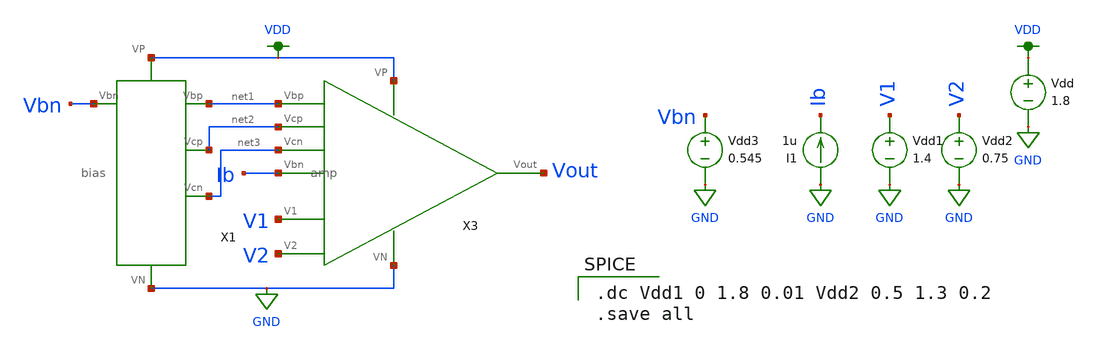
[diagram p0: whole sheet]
** sch_path: mp3/schematic/lds/amp_tran_lds.sch
**.subckt amp_tran_lds
Vdd1 V1 GND 1.4
Vdd2 V2 GND 0.75
I1 GND Ib 1u
Vdd VDD GND 1.8
Vdd3 Vbn GND 0.545
X3 VDD GND Ib net3 net2 net1 V1 V2 Vout amp
X1 VDD GND Vbn net1 net2 net3 bias
**** begin user architecture code

.option wnflag=1
.lib ~/skywater/skywater-pdk/libraries/sky130_fd_pr_ngspice/latest/models/sky130.lib.spice tt


.dc Vdd1 0 1.8 0.01 Vdd2 0.5 1.3 0.2
.save all

**** end user architecture code
**.ends

* expanding   symbol:  /home/madvlsi/madvlsi/mp3/schematic/lds/amp.sym # of pins=9
** sym_path: mp3/schematic/lds/amp.sym
** sch_path: mp3/schematic/lds/amp.sch
.subckt amp VP VN Vbn Vcn Vcp Vbp V1 V2 Vout
*.iopin VP
*.iopin VN
*.opin Vout
*.ipin V1
*.ipin V2
*.ipin Vbp
*.ipin Vcp
*.iopin Vbn
*.ipin Vcn
XM95 net2 Vcp net1 VDD sky130_fd_pr__pfet_01v8 L=0.5 W=6 nf=1 ad='int((nf+1)/2) * W/nf * 0.29' as='int((nf+2)/2) * W/nf * 0.29'
+ pd='2*int((nf+1)/2) * (W/nf + 0.29)' ps='2*int((nf+2)/2) * (W/nf + 0.29)' nrd='0.29 / W' nrs='0.29 / W'
+ sa=0 sb=0 sd=0 mult=1 m=1
XM96 net1 Vcp net2 VDD sky130_fd_pr__pfet_01v8 L=0.5 W=6 nf=1 ad='int((nf+1)/2) * W/nf * 0.29' as='int((nf+2)/2) * W/nf * 0.29'
+ pd='2*int((nf+1)/2) * (W/nf + 0.29)' ps='2*int((nf+2)/2) * (W/nf + 0.29)' nrd='0.29 / W' nrs='0.29 / W'
+ sa=0 sb=0 sd=0 mult=1 m=1
XM911 VP Vbp net2 VDD sky130_fd_pr__pfet_01v8 L=0.5 W=6 nf=1 ad='int((nf+1)/2) * W/nf * 0.29' as='int((nf+2)/2) * W/nf * 0.29'
+ pd='2*int((nf+1)/2) * (W/nf + 0.29)' ps='2*int((nf+2)/2) * (W/nf + 0.29)' nrd='0.29 / W' nrs='0.29 / W'
+ sa=0 sb=0 sd=0 mult=1 m=1
XM912 net2 Vbp VP VDD sky130_fd_pr__pfet_01v8 L=0.5 W=6 nf=1 ad='int((nf+1)/2) * W/nf * 0.29' as='int((nf+2)/2) * W/nf * 0.29'
+ pd='2*int((nf+1)/2) * (W/nf + 0.29)' ps='2*int((nf+2)/2) * (W/nf + 0.29)' nrd='0.29 / W' nrs='0.29 / W'
+ sa=0 sb=0 sd=0 mult=1 m=1
XM913 VP Vbp net3 VDD sky130_fd_pr__pfet_01v8 L=0.5 W=6 nf=1 ad='int((nf+1)/2) * W/nf * 0.29' as='int((nf+2)/2) * W/nf * 0.29'
+ pd='2*int((nf+1)/2) * (W/nf + 0.29)' ps='2*int((nf+2)/2) * (W/nf + 0.29)' nrd='0.29 / W' nrs='0.29 / W'
+ sa=0 sb=0 sd=0 mult=1 m=1
XM914 net3 Vbp VP VDD sky130_fd_pr__pfet_01v8 L=0.5 W=6 nf=1 ad='int((nf+1)/2) * W/nf * 0.29' as='int((nf+2)/2) * W/nf * 0.29'
+ pd='2*int((nf+1)/2) * (W/nf + 0.29)' ps='2*int((nf+2)/2) * (W/nf + 0.29)' nrd='0.29 / W' nrs='0.29 / W'
+ sa=0 sb=0 sd=0 mult=1 m=1
XM915 net3 Vcp Vout VDD sky130_fd_pr__pfet_01v8 L=0.5 W=6 nf=1 ad='int((nf+1)/2) * W/nf * 0.29' as='int((nf+2)/2) * W/nf * 0.29'
+ pd='2*int((nf+1)/2) * (W/nf + 0.29)' ps='2*int((nf+2)/2) * (W/nf + 0.29)' nrd='0.29 / W' nrs='0.29 / W'
+ sa=0 sb=0 sd=0 mult=1 m=1
XM916 Vout Vcp net3 VDD sky130_fd_pr__pfet_01v8 L=0.5 W=6 nf=1 ad='int((nf+1)/2) * W/nf * 0.29' as='int((nf+2)/2) * W/nf * 0.29'
+ pd='2*int((nf+1)/2) * (W/nf + 0.29)' ps='2*int((nf+2)/2) * (W/nf + 0.29)' nrd='0.29 / W' nrs='0.29 / W'
+ sa=0 sb=0 sd=0 mult=1 m=1
XM917 net2 V1 net4 GND sky130_fd_pr__nfet_01v8 L=0.5 W=3 nf=1 ad='int((nf+1)/2) * W/nf * 0.29' as='int((nf+2)/2) * W/nf * 0.29'
+ pd='2*int((nf+1)/2) * (W/nf + 0.29)' ps='2*int((nf+2)/2) * (W/nf + 0.29)' nrd='0.29 / W' nrs='0.29 / W'
+ sa=0 sb=0 sd=0 mult=1 m=1
XM918 net4 V1 net2 GND sky130_fd_pr__nfet_01v8 L=0.5 W=3 nf=1 ad='int((nf+1)/2) * W/nf * 0.29' as='int((nf+2)/2) * W/nf * 0.29'
+ pd='2*int((nf+1)/2) * (W/nf + 0.29)' ps='2*int((nf+2)/2) * (W/nf + 0.29)' nrd='0.29 / W' nrs='0.29 / W'
+ sa=0 sb=0 sd=0 mult=1 m=1
XM919 net2 V1 net4 GND sky130_fd_pr__nfet_01v8 L=0.5 W=3 nf=1 ad='int((nf+1)/2) * W/nf * 0.29' as='int((nf+2)/2) * W/nf * 0.29'
+ pd='2*int((nf+1)/2) * (W/nf + 0.29)' ps='2*int((nf+2)/2) * (W/nf + 0.29)' nrd='0.29 / W' nrs='0.29 / W'
+ sa=0 sb=0 sd=0 mult=1 m=1
XM920 net4 V1 net2 GND sky130_fd_pr__nfet_01v8 L=0.5 W=3 nf=1 ad='int((nf+1)/2) * W/nf * 0.29' as='int((nf+2)/2) * W/nf * 0.29'
+ pd='2*int((nf+1)/2) * (W/nf + 0.29)' ps='2*int((nf+2)/2) * (W/nf + 0.29)' nrd='0.29 / W' nrs='0.29 / W'
+ sa=0 sb=0 sd=0 mult=1 m=1
XM921 net3 V2 net4 GND sky130_fd_pr__nfet_01v8 L=0.5 W=3 nf=1 ad='int((nf+1)/2) * W/nf * 0.29' as='int((nf+2)/2) * W/nf * 0.29'
+ pd='2*int((nf+1)/2) * (W/nf + 0.29)' ps='2*int((nf+2)/2) * (W/nf + 0.29)' nrd='0.29 / W' nrs='0.29 / W'
+ sa=0 sb=0 sd=0 mult=1 m=1
XM922 net4 V2 net3 GND sky130_fd_pr__nfet_01v8 L=0.5 W=3 nf=1 ad='int((nf+1)/2) * W/nf * 0.29' as='int((nf+2)/2) * W/nf * 0.29'
+ pd='2*int((nf+1)/2) * (W/nf + 0.29)' ps='2*int((nf+2)/2) * (W/nf + 0.29)' nrd='0.29 / W' nrs='0.29 / W'
+ sa=0 sb=0 sd=0 mult=1 m=1
XM923 net3 V2 net4 GND sky130_fd_pr__nfet_01v8 L=0.5 W=3 nf=1 ad='int((nf+1)/2) * W/nf * 0.29' as='int((nf+2)/2) * W/nf * 0.29'
+ pd='2*int((nf+1)/2) * (W/nf + 0.29)' ps='2*int((nf+2)/2) * (W/nf + 0.29)' nrd='0.29 / W' nrs='0.29 / W'
+ sa=0 sb=0 sd=0 mult=1 m=1
XM94 net4 V2 net3 GND sky130_fd_pr__nfet_01v8 L=0.5 W=3 nf=1 ad='int((nf+1)/2) * W/nf * 0.29' as='int((nf+2)/2) * W/nf * 0.29'
+ pd='2*int((nf+1)/2) * (W/nf + 0.29)' ps='2*int((nf+2)/2) * (W/nf + 0.29)' nrd='0.29 / W' nrs='0.29 / W'
+ sa=0 sb=0 sd=0 mult=1 m=1
XM925 VN Vbn Vbn GND sky130_fd_pr__nfet_01v8 L=0.5 W=6 nf=1 ad='int((nf+1)/2) * W/nf * 0.29' as='int((nf+2)/2) * W/nf * 0.29'
+ pd='2*int((nf+1)/2) * (W/nf + 0.29)' ps='2*int((nf+2)/2) * (W/nf + 0.29)' nrd='0.29 / W' nrs='0.29 / W'
+ sa=0 sb=0 sd=0 mult=1 m=1
XM926 Vbn Vbn VN GND sky130_fd_pr__nfet_01v8 L=0.5 W=6 nf=1 ad='int((nf+1)/2) * W/nf * 0.29' as='int((nf+2)/2) * W/nf * 0.29'
+ pd='2*int((nf+1)/2) * (W/nf + 0.29)' ps='2*int((nf+2)/2) * (W/nf + 0.29)' nrd='0.29 / W' nrs='0.29 / W'
+ sa=0 sb=0 sd=0 mult=1 m=1
XM927 VN Vbn net4 GND sky130_fd_pr__nfet_01v8 L=0.5 W=6 nf=1 ad='int((nf+1)/2) * W/nf * 0.29' as='int((nf+2)/2) * W/nf * 0.29'
+ pd='2*int((nf+1)/2) * (W/nf + 0.29)' ps='2*int((nf+2)/2) * (W/nf + 0.29)' nrd='0.29 / W' nrs='0.29 / W'
+ sa=0 sb=0 sd=0 mult=1 m=1
XM928 net4 Vbn VN GND sky130_fd_pr__nfet_01v8 L=0.5 W=6 nf=1 ad='int((nf+1)/2) * W/nf * 0.29' as='int((nf+2)/2) * W/nf * 0.29'
+ pd='2*int((nf+1)/2) * (W/nf + 0.29)' ps='2*int((nf+2)/2) * (W/nf + 0.29)' nrd='0.29 / W' nrs='0.29 / W'
+ sa=0 sb=0 sd=0 mult=1 m=1
XM929 VN Vbn Vbn GND sky130_fd_pr__nfet_01v8 L=0.5 W=6 nf=1 ad='int((nf+1)/2) * W/nf * 0.29' as='int((nf+2)/2) * W/nf * 0.29'
+ pd='2*int((nf+1)/2) * (W/nf + 0.29)' ps='2*int((nf+2)/2) * (W/nf + 0.29)' nrd='0.29 / W' nrs='0.29 / W'
+ sa=0 sb=0 sd=0 mult=1 m=1
XM930 Vbn Vbn VN GND sky130_fd_pr__nfet_01v8 L=0.5 W=6 nf=1 ad='int((nf+1)/2) * W/nf * 0.29' as='int((nf+2)/2) * W/nf * 0.29'
+ pd='2*int((nf+1)/2) * (W/nf + 0.29)' ps='2*int((nf+2)/2) * (W/nf + 0.29)' nrd='0.29 / W' nrs='0.29 / W'
+ sa=0 sb=0 sd=0 mult=1 m=1
XM931 VN Vbn net4 GND sky130_fd_pr__nfet_01v8 L=0.5 W=6 nf=1 ad='int((nf+1)/2) * W/nf * 0.29' as='int((nf+2)/2) * W/nf * 0.29'
+ pd='2*int((nf+1)/2) * (W/nf + 0.29)' ps='2*int((nf+2)/2) * (W/nf + 0.29)' nrd='0.29 / W' nrs='0.29 / W'
+ sa=0 sb=0 sd=0 mult=1 m=1
XM932 net4 Vbn VN GND sky130_fd_pr__nfet_01v8 L=0.5 W=6 nf=1 ad='int((nf+1)/2) * W/nf * 0.29' as='int((nf+2)/2) * W/nf * 0.29'
+ pd='2*int((nf+1)/2) * (W/nf + 0.29)' ps='2*int((nf+2)/2) * (W/nf + 0.29)' nrd='0.29 / W' nrs='0.29 / W'
+ sa=0 sb=0 sd=0 mult=1 m=1
XM933 net5 Vcn net1 GND sky130_fd_pr__nfet_01v8 L=0.5 W=6 nf=1 ad='int((nf+1)/2) * W/nf * 0.29' as='int((nf+2)/2) * W/nf * 0.29'
+ pd='2*int((nf+1)/2) * (W/nf + 0.29)' ps='2*int((nf+2)/2) * (W/nf + 0.29)' nrd='0.29 / W' nrs='0.29 / W'
+ sa=0 sb=0 sd=0 mult=1 m=1
XM934 net1 Vcn net5 GND sky130_fd_pr__nfet_01v8 L=0.5 W=6 nf=1 ad='int((nf+1)/2) * W/nf * 0.29' as='int((nf+2)/2) * W/nf * 0.29'
+ pd='2*int((nf+1)/2) * (W/nf + 0.29)' ps='2*int((nf+2)/2) * (W/nf + 0.29)' nrd='0.29 / W' nrs='0.29 / W'
+ sa=0 sb=0 sd=0 mult=1 m=1
XM935 net5 net1 VN GND sky130_fd_pr__nfet_01v8 L=0.5 W=6 nf=1 ad='int((nf+1)/2) * W/nf * 0.29' as='int((nf+2)/2) * W/nf * 0.29'
+ pd='2*int((nf+1)/2) * (W/nf + 0.29)' ps='2*int((nf+2)/2) * (W/nf + 0.29)' nrd='0.29 / W' nrs='0.29 / W'
+ sa=0 sb=0 sd=0 mult=1 m=1
XM936 VN net1 net5 GND sky130_fd_pr__nfet_01v8 L=0.5 W=6 nf=1 ad='int((nf+1)/2) * W/nf * 0.29' as='int((nf+2)/2) * W/nf * 0.29'
+ pd='2*int((nf+1)/2) * (W/nf + 0.29)' ps='2*int((nf+2)/2) * (W/nf + 0.29)' nrd='0.29 / W' nrs='0.29 / W'
+ sa=0 sb=0 sd=0 mult=1 m=1
XM937 net6 Vcn Vout GND sky130_fd_pr__nfet_01v8 L=0.5 W=6 nf=1 ad='int((nf+1)/2) * W/nf * 0.29' as='int((nf+2)/2) * W/nf * 0.29'
+ pd='2*int((nf+1)/2) * (W/nf + 0.29)' ps='2*int((nf+2)/2) * (W/nf + 0.29)' nrd='0.29 / W' nrs='0.29 / W'
+ sa=0 sb=0 sd=0 mult=1 m=1
XM938 Vout Vcn net6 GND sky130_fd_pr__nfet_01v8 L=0.5 W=6 nf=1 ad='int((nf+1)/2) * W/nf * 0.29' as='int((nf+2)/2) * W/nf * 0.29'
+ pd='2*int((nf+1)/2) * (W/nf + 0.29)' ps='2*int((nf+2)/2) * (W/nf + 0.29)' nrd='0.29 / W' nrs='0.29 / W'
+ sa=0 sb=0 sd=0 mult=1 m=1
XM939 net6 net1 VN GND sky130_fd_pr__nfet_01v8 L=0.5 W=6 nf=1 ad='int((nf+1)/2) * W/nf * 0.29' as='int((nf+2)/2) * W/nf * 0.29'
+ pd='2*int((nf+1)/2) * (W/nf + 0.29)' ps='2*int((nf+2)/2) * (W/nf + 0.29)' nrd='0.29 / W' nrs='0.29 / W'
+ sa=0 sb=0 sd=0 mult=1 m=1
XM940 VN net1 net6 GND sky130_fd_pr__nfet_01v8 L=0.5 W=6 nf=1 ad='int((nf+1)/2) * W/nf * 0.29' as='int((nf+2)/2) * W/nf * 0.29'
+ pd='2*int((nf+1)/2) * (W/nf + 0.29)' ps='2*int((nf+2)/2) * (W/nf + 0.29)' nrd='0.29 / W' nrs='0.29 / W'
+ sa=0 sb=0 sd=0 mult=1 m=1
XM1 VN VN Vbn GND sky130_fd_pr__nfet_01v8 L=0.5 W=6 nf=1 ad='int((nf+1)/2) * W/nf * 0.29' as='int((nf+2)/2) * W/nf * 0.29'
+ pd='2*int((nf+1)/2) * (W/nf + 0.29)' ps='2*int((nf+2)/2) * (W/nf + 0.29)' nrd='0.29 / W' nrs='0.29 / W'
+ sa=0 sb=0 sd=0 mult=1 m=1
XM2 net1 VN VN GND sky130_fd_pr__nfet_01v8 L=0.5 W=6 nf=1 ad='int((nf+1)/2) * W/nf * 0.29' as='int((nf+2)/2) * W/nf * 0.29'
+ pd='2*int((nf+1)/2) * (W/nf + 0.29)' ps='2*int((nf+2)/2) * (W/nf + 0.29)' nrd='0.29 / W' nrs='0.29 / W'
+ sa=0 sb=0 sd=0 mult=1 m=1
XM3 VN VN net4 GND sky130_fd_pr__nfet_01v8 L=0.5 W=3 nf=1 ad='int((nf+1)/2) * W/nf * 0.29' as='int((nf+2)/2) * W/nf * 0.29'
+ pd='2*int((nf+1)/2) * (W/nf + 0.29)' ps='2*int((nf+2)/2) * (W/nf + 0.29)' nrd='0.29 / W' nrs='0.29 / W'
+ sa=0 sb=0 sd=0 mult=1 m=1
XM4 VP VP net2 VDD sky130_fd_pr__pfet_01v8 L=0.5 W=6 nf=1 ad='int((nf+1)/2) * W/nf * 0.29' as='int((nf+2)/2) * W/nf * 0.29'
+ pd='2*int((nf+1)/2) * (W/nf + 0.29)' ps='2*int((nf+2)/2) * (W/nf + 0.29)' nrd='0.29 / W' nrs='0.29 / W'
+ sa=0 sb=0 sd=0 mult=1 m=1
XM5 net3 VP VP VDD sky130_fd_pr__pfet_01v8 L=0.5 W=6 nf=1 ad='int((nf+1)/2) * W/nf * 0.29' as='int((nf+2)/2) * W/nf * 0.29'
+ pd='2*int((nf+1)/2) * (W/nf + 0.29)' ps='2*int((nf+2)/2) * (W/nf + 0.29)' nrd='0.29 / W' nrs='0.29 / W'
+ sa=0 sb=0 sd=0 mult=1 m=1
XM6 net4 VN VN GND sky130_fd_pr__nfet_01v8 L=0.5 W=3 nf=1 ad='int((nf+1)/2) * W/nf * 0.29' as='int((nf+2)/2) * W/nf * 0.29'
+ pd='2*int((nf+1)/2) * (W/nf + 0.29)' ps='2*int((nf+2)/2) * (W/nf + 0.29)' nrd='0.29 / W' nrs='0.29 / W'
+ sa=0 sb=0 sd=0 mult=1 m=1
XM7 Vbn VN VN GND sky130_fd_pr__nfet_01v8 L=0.5 W=3 nf=1 ad='int((nf+1)/2) * W/nf * 0.29' as='int((nf+2)/2) * W/nf * 0.29'
+ pd='2*int((nf+1)/2) * (W/nf + 0.29)' ps='2*int((nf+2)/2) * (W/nf + 0.29)' nrd='0.29 / W' nrs='0.29 / W'
+ sa=0 sb=0 sd=0 mult=1 m=1
XM8 Vout VN VN GND sky130_fd_pr__nfet_01v8 L=0.5 W=6 nf=1 ad='int((nf+1)/2) * W/nf * 0.29' as='int((nf+2)/2) * W/nf * 0.29'
+ pd='2*int((nf+1)/2) * (W/nf + 0.29)' ps='2*int((nf+2)/2) * (W/nf + 0.29)' nrd='0.29 / W' nrs='0.29 / W'
+ sa=0 sb=0 sd=0 mult=1 m=1
.ends


* expanding   symbol:  /home/madvlsi/madvlsi/mp3/schematic/lds/bias.sym # of pins=6
** sym_path: mp3/schematic/lds/bias.sym
** sch_path: mp3/schematic/lds/bias.sch
.subckt bias VP VN Vbn Vbp Vcp Vcn
*.iopin VP
*.iopin VN
*.iopin Vbn
*.opin Vcn
*.opin Vcp
*.opin Vbp
XM1 VP Vbp net5 VDD sky130_fd_pr__pfet_01v8 L=0.5 W=6 nf=1 ad='int((nf+1)/2) * W/nf * 0.29' as='int((nf+2)/2) * W/nf * 0.29'
+ pd='2*int((nf+1)/2) * (W/nf + 0.29)' ps='2*int((nf+2)/2) * (W/nf + 0.29)' nrd='0.29 / W' nrs='0.29 / W'
+ sa=0 sb=0 sd=0 mult=1 m=1
XM2 net5 Vbp net4 VDD sky130_fd_pr__pfet_01v8 L=0.5 W=6 nf=1 ad='int((nf+1)/2) * W/nf * 0.29' as='int((nf+2)/2) * W/nf * 0.29'
+ pd='2*int((nf+1)/2) * (W/nf + 0.29)' ps='2*int((nf+2)/2) * (W/nf + 0.29)' nrd='0.29 / W' nrs='0.29 / W'
+ sa=0 sb=0 sd=0 mult=1 m=1
XM3 net4 Vbp net3 VDD sky130_fd_pr__pfet_01v8 L=0.5 W=6 nf=1 ad='int((nf+1)/2) * W/nf * 0.29' as='int((nf+2)/2) * W/nf * 0.29'
+ pd='2*int((nf+1)/2) * (W/nf + 0.29)' ps='2*int((nf+2)/2) * (W/nf + 0.29)' nrd='0.29 / W' nrs='0.29 / W'
+ sa=0 sb=0 sd=0 mult=1 m=1
XM4 net3 Vbp net2 VDD sky130_fd_pr__pfet_01v8 L=0.5 W=6 nf=1 ad='int((nf+1)/2) * W/nf * 0.29' as='int((nf+2)/2) * W/nf * 0.29'
+ pd='2*int((nf+1)/2) * (W/nf + 0.29)' ps='2*int((nf+2)/2) * (W/nf + 0.29)' nrd='0.29 / W' nrs='0.29 / W'
+ sa=0 sb=0 sd=0 mult=1 m=1
XM5 net2 Vbp net1 VDD sky130_fd_pr__pfet_01v8 L=0.5 W=6 nf=1 ad='int((nf+1)/2) * W/nf * 0.29' as='int((nf+2)/2) * W/nf * 0.29'
+ pd='2*int((nf+1)/2) * (W/nf + 0.29)' ps='2*int((nf+2)/2) * (W/nf + 0.29)' nrd='0.29 / W' nrs='0.29 / W'
+ sa=0 sb=0 sd=0 mult=1 m=1
XM6 net1 Vbp net13 VDD sky130_fd_pr__pfet_01v8 L=0.5 W=6 nf=1 ad='int((nf+1)/2) * W/nf * 0.29' as='int((nf+2)/2) * W/nf * 0.29'
+ pd='2*int((nf+1)/2) * (W/nf + 0.29)' ps='2*int((nf+2)/2) * (W/nf + 0.29)' nrd='0.29 / W' nrs='0.29 / W'
+ sa=0 sb=0 sd=0 mult=1 m=1
XM7 net7 Vbn net6 GND sky130_fd_pr__nfet_01v8 L=0.5 W=6 nf=1 ad='int((nf+1)/2) * W/nf * 0.29' as='int((nf+2)/2) * W/nf * 0.29'
+ pd='2*int((nf+1)/2) * (W/nf + 0.29)' ps='2*int((nf+2)/2) * (W/nf + 0.29)' nrd='0.29 / W' nrs='0.29 / W'
+ sa=0 sb=0 sd=0 mult=1 m=1
XM8 net6 Vbn VN GND sky130_fd_pr__nfet_01v8 L=0.5 W=6 nf=1 ad='int((nf+1)/2) * W/nf * 0.29' as='int((nf+2)/2) * W/nf * 0.29'
+ pd='2*int((nf+1)/2) * (W/nf + 0.29)' ps='2*int((nf+2)/2) * (W/nf + 0.29)' nrd='0.29 / W' nrs='0.29 / W'
+ sa=0 sb=0 sd=0 mult=1 m=1
XM9 net8 Vbn net7 GND sky130_fd_pr__nfet_01v8 L=0.5 W=6 nf=1 ad='int((nf+1)/2) * W/nf * 0.29' as='int((nf+2)/2) * W/nf * 0.29'
+ pd='2*int((nf+1)/2) * (W/nf + 0.29)' ps='2*int((nf+2)/2) * (W/nf + 0.29)' nrd='0.29 / W' nrs='0.29 / W'
+ sa=0 sb=0 sd=0 mult=1 m=1
XM10 net9 Vbn net8 GND sky130_fd_pr__nfet_01v8 L=0.5 W=6 nf=1 ad='int((nf+1)/2) * W/nf * 0.29' as='int((nf+2)/2) * W/nf * 0.29'
+ pd='2*int((nf+1)/2) * (W/nf + 0.29)' ps='2*int((nf+2)/2) * (W/nf + 0.29)' nrd='0.29 / W' nrs='0.29 / W'
+ sa=0 sb=0 sd=0 mult=1 m=1
XM11 net10 Vbn net9 GND sky130_fd_pr__nfet_01v8 L=0.5 W=6 nf=1 ad='int((nf+1)/2) * W/nf * 0.29' as='int((nf+2)/2) * W/nf * 0.29'
+ pd='2*int((nf+1)/2) * (W/nf + 0.29)' ps='2*int((nf+2)/2) * (W/nf + 0.29)' nrd='0.29 / W' nrs='0.29 / W'
+ sa=0 sb=0 sd=0 mult=1 m=1
XM12 net11 Vbn net10 GND sky130_fd_pr__nfet_01v8 L=0.5 W=6 nf=1 ad='int((nf+1)/2) * W/nf * 0.29' as='int((nf+2)/2) * W/nf * 0.29'
+ pd='2*int((nf+1)/2) * (W/nf + 0.29)' ps='2*int((nf+2)/2) * (W/nf + 0.29)' nrd='0.29 / W' nrs='0.29 / W'
+ sa=0 sb=0 sd=0 mult=1 m=1
XM13 net11 net11 net12 VDD sky130_fd_pr__pfet_01v8 L=0.5 W=6 nf=1 ad='int((nf+1)/2) * W/nf * 0.29' as='int((nf+2)/2) * W/nf * 0.29'
+ pd='2*int((nf+1)/2) * (W/nf + 0.29)' ps='2*int((nf+2)/2) * (W/nf + 0.29)' nrd='0.29 / W' nrs='0.29 / W'
+ sa=0 sb=0 sd=0 mult=1 m=1
XM14 net12 net11 net11 VDD sky130_fd_pr__pfet_01v8 L=0.5 W=6 nf=1 ad='int((nf+1)/2) * W/nf * 0.29' as='int((nf+2)/2) * W/nf * 0.29'
+ pd='2*int((nf+1)/2) * (W/nf + 0.29)' ps='2*int((nf+2)/2) * (W/nf + 0.29)' nrd='0.29 / W' nrs='0.29 / W'
+ sa=0 sb=0 sd=0 mult=1 m=1
XM15 net11 net11 net12 VDD sky130_fd_pr__pfet_01v8 L=0.5 W=6 nf=1 ad='int((nf+1)/2) * W/nf * 0.29' as='int((nf+2)/2) * W/nf * 0.29'
+ pd='2*int((nf+1)/2) * (W/nf + 0.29)' ps='2*int((nf+2)/2) * (W/nf + 0.29)' nrd='0.29 / W' nrs='0.29 / W'
+ sa=0 sb=0 sd=0 mult=1 m=1
XM16 net12 net11 net11 VDD sky130_fd_pr__pfet_01v8 L=0.5 W=6 nf=1 ad='int((nf+1)/2) * W/nf * 0.29' as='int((nf+2)/2) * W/nf * 0.29'
+ pd='2*int((nf+1)/2) * (W/nf + 0.29)' ps='2*int((nf+2)/2) * (W/nf + 0.29)' nrd='0.29 / W' nrs='0.29 / W'
+ sa=0 sb=0 sd=0 mult=1 m=1
XM17 net13 net13 net14 GND sky130_fd_pr__nfet_01v8 L=0.5 W=6 nf=1 ad='int((nf+1)/2) * W/nf * 0.29' as='int((nf+2)/2) * W/nf * 0.29'
+ pd='2*int((nf+1)/2) * (W/nf + 0.29)' ps='2*int((nf+2)/2) * (W/nf + 0.29)' nrd='0.29 / W' nrs='0.29 / W'
+ sa=0 sb=0 sd=0 mult=1 m=1
XM18 net14 net13 net13 GND sky130_fd_pr__nfet_01v8 L=0.5 W=6 nf=1 ad='int((nf+1)/2) * W/nf * 0.29' as='int((nf+2)/2) * W/nf * 0.29'
+ pd='2*int((nf+1)/2) * (W/nf + 0.29)' ps='2*int((nf+2)/2) * (W/nf + 0.29)' nrd='0.29 / W' nrs='0.29 / W'
+ sa=0 sb=0 sd=0 mult=1 m=1
XM19 net13 net13 net14 GND sky130_fd_pr__nfet_01v8 L=0.5 W=6 nf=1 ad='int((nf+1)/2) * W/nf * 0.29' as='int((nf+2)/2) * W/nf * 0.29'
+ pd='2*int((nf+1)/2) * (W/nf + 0.29)' ps='2*int((nf+2)/2) * (W/nf + 0.29)' nrd='0.29 / W' nrs='0.29 / W'
+ sa=0 sb=0 sd=0 mult=1 m=1
XM20 net14 net13 net13 GND sky130_fd_pr__nfet_01v8 L=0.5 W=6 nf=1 ad='int((nf+1)/2) * W/nf * 0.29' as='int((nf+2)/2) * W/nf * 0.29'
+ pd='2*int((nf+1)/2) * (W/nf + 0.29)' ps='2*int((nf+2)/2) * (W/nf + 0.29)' nrd='0.29 / W' nrs='0.29 / W'
+ sa=0 sb=0 sd=0 mult=1 m=1
XM21 Vcn Vbp VP VDD sky130_fd_pr__pfet_01v8 L=0.5 W=6 nf=1 ad='int((nf+1)/2) * W/nf * 0.29' as='int((nf+2)/2) * W/nf * 0.29'
+ pd='2*int((nf+1)/2) * (W/nf + 0.29)' ps='2*int((nf+2)/2) * (W/nf + 0.29)' nrd='0.29 / W' nrs='0.29 / W'
+ sa=0 sb=0 sd=0 mult=1 m=1
XM22 Vcn Vcn net14 GND sky130_fd_pr__nfet_01v8 L=0.5 W=6 nf=1 ad='int((nf+1)/2) * W/nf * 0.29' as='int((nf+2)/2) * W/nf * 0.29'
+ pd='2*int((nf+1)/2) * (W/nf + 0.29)' ps='2*int((nf+2)/2) * (W/nf + 0.29)' nrd='0.29 / W' nrs='0.29 / W'
+ sa=0 sb=0 sd=0 mult=1 m=1
XM23 VN net13 net14 GND sky130_fd_pr__nfet_01v8 L=0.5 W=6 nf=1 ad='int((nf+1)/2) * W/nf * 0.29' as='int((nf+2)/2) * W/nf * 0.29'
+ pd='2*int((nf+1)/2) * (W/nf + 0.29)' ps='2*int((nf+2)/2) * (W/nf + 0.29)' nrd='0.29 / W' nrs='0.29 / W'
+ sa=0 sb=0 sd=0 mult=1 m=1
XM24 VN Vbn Vcp GND sky130_fd_pr__nfet_01v8 L=0.5 W=6 nf=1 ad='int((nf+1)/2) * W/nf * 0.29' as='int((nf+2)/2) * W/nf * 0.29'
+ pd='2*int((nf+1)/2) * (W/nf + 0.29)' ps='2*int((nf+2)/2) * (W/nf + 0.29)' nrd='0.29 / W' nrs='0.29 / W'
+ sa=0 sb=0 sd=0 mult=1 m=1
XM25 net12 Vcp Vcp VDD sky130_fd_pr__pfet_01v8 L=0.5 W=6 nf=1 ad='int((nf+1)/2) * W/nf * 0.29' as='int((nf+2)/2) * W/nf * 0.29'
+ pd='2*int((nf+1)/2) * (W/nf + 0.29)' ps='2*int((nf+2)/2) * (W/nf + 0.29)' nrd='0.29 / W' nrs='0.29 / W'
+ sa=0 sb=0 sd=0 mult=1 m=1
XM26 net12 net11 VP VDD sky130_fd_pr__pfet_01v8 L=0.5 W=6 nf=1 ad='int((nf+1)/2) * W/nf * 0.29' as='int((nf+2)/2) * W/nf * 0.29'
+ pd='2*int((nf+1)/2) * (W/nf + 0.29)' ps='2*int((nf+2)/2) * (W/nf + 0.29)' nrd='0.29 / W' nrs='0.29 / W'
+ sa=0 sb=0 sd=0 mult=1 m=1
XM27 Vbp Vbp VP VDD sky130_fd_pr__pfet_01v8 L=0.5 W=6 nf=1 ad='int((nf+1)/2) * W/nf * 0.29' as='int((nf+2)/2) * W/nf * 0.29'
+ pd='2*int((nf+1)/2) * (W/nf + 0.29)' ps='2*int((nf+2)/2) * (W/nf + 0.29)' nrd='0.29 / W' nrs='0.29 / W'
+ sa=0 sb=0 sd=0 mult=1 m=1
XM28 VN Vbn Vbp GND sky130_fd_pr__nfet_01v8 L=0.5 W=6 nf=1 ad='int((nf+1)/2) * W/nf * 0.29' as='int((nf+2)/2) * W/nf * 0.29'
+ pd='2*int((nf+1)/2) * (W/nf + 0.29)' ps='2*int((nf+2)/2) * (W/nf + 0.29)' nrd='0.29 / W' nrs='0.29 / W'
+ sa=0 sb=0 sd=0 mult=1 m=1
XM29 VP Vbp net19 VDD sky130_fd_pr__pfet_01v8 L=0.5 W=6 nf=1 ad='int((nf+1)/2) * W/nf * 0.29' as='int((nf+2)/2) * W/nf * 0.29'
+ pd='2*int((nf+1)/2) * (W/nf + 0.29)' ps='2*int((nf+2)/2) * (W/nf + 0.29)' nrd='0.29 / W' nrs='0.29 / W'
+ sa=0 sb=0 sd=0 mult=1 m=1
XM30 net19 Vbp net18 VDD sky130_fd_pr__pfet_01v8 L=0.5 W=6 nf=1 ad='int((nf+1)/2) * W/nf * 0.29' as='int((nf+2)/2) * W/nf * 0.29'
+ pd='2*int((nf+1)/2) * (W/nf + 0.29)' ps='2*int((nf+2)/2) * (W/nf + 0.29)' nrd='0.29 / W' nrs='0.29 / W'
+ sa=0 sb=0 sd=0 mult=1 m=1
XM31 net18 Vbp net17 VDD sky130_fd_pr__pfet_01v8 L=0.5 W=6 nf=1 ad='int((nf+1)/2) * W/nf * 0.29' as='int((nf+2)/2) * W/nf * 0.29'
+ pd='2*int((nf+1)/2) * (W/nf + 0.29)' ps='2*int((nf+2)/2) * (W/nf + 0.29)' nrd='0.29 / W' nrs='0.29 / W'
+ sa=0 sb=0 sd=0 mult=1 m=1
XM32 net17 Vbp net16 VDD sky130_fd_pr__pfet_01v8 L=0.5 W=6 nf=1 ad='int((nf+1)/2) * W/nf * 0.29' as='int((nf+2)/2) * W/nf * 0.29'
+ pd='2*int((nf+1)/2) * (W/nf + 0.29)' ps='2*int((nf+2)/2) * (W/nf + 0.29)' nrd='0.29 / W' nrs='0.29 / W'
+ sa=0 sb=0 sd=0 mult=1 m=1
XM33 net16 Vbp net15 VDD sky130_fd_pr__pfet_01v8 L=0.5 W=6 nf=1 ad='int((nf+1)/2) * W/nf * 0.29' as='int((nf+2)/2) * W/nf * 0.29'
+ pd='2*int((nf+1)/2) * (W/nf + 0.29)' ps='2*int((nf+2)/2) * (W/nf + 0.29)' nrd='0.29 / W' nrs='0.29 / W'
+ sa=0 sb=0 sd=0 mult=1 m=1
XM34 net15 Vbp net13 VDD sky130_fd_pr__pfet_01v8 L=0.5 W=6 nf=1 ad='int((nf+1)/2) * W/nf * 0.29' as='int((nf+2)/2) * W/nf * 0.29'
+ pd='2*int((nf+1)/2) * (W/nf + 0.29)' ps='2*int((nf+2)/2) * (W/nf + 0.29)' nrd='0.29 / W' nrs='0.29 / W'
+ sa=0 sb=0 sd=0 mult=1 m=1
XM35 net21 Vbn net20 GND sky130_fd_pr__nfet_01v8 L=0.5 W=6 nf=1 ad='int((nf+1)/2) * W/nf * 0.29' as='int((nf+2)/2) * W/nf * 0.29'
+ pd='2*int((nf+1)/2) * (W/nf + 0.29)' ps='2*int((nf+2)/2) * (W/nf + 0.29)' nrd='0.29 / W' nrs='0.29 / W'
+ sa=0 sb=0 sd=0 mult=1 m=1
XM36 net20 Vbn VN GND sky130_fd_pr__nfet_01v8 L=0.5 W=6 nf=1 ad='int((nf+1)/2) * W/nf * 0.29' as='int((nf+2)/2) * W/nf * 0.29'
+ pd='2*int((nf+1)/2) * (W/nf + 0.29)' ps='2*int((nf+2)/2) * (W/nf + 0.29)' nrd='0.29 / W' nrs='0.29 / W'
+ sa=0 sb=0 sd=0 mult=1 m=1
XM37 net22 Vbn net21 GND sky130_fd_pr__nfet_01v8 L=0.5 W=6 nf=1 ad='int((nf+1)/2) * W/nf * 0.29' as='int((nf+2)/2) * W/nf * 0.29'
+ pd='2*int((nf+1)/2) * (W/nf + 0.29)' ps='2*int((nf+2)/2) * (W/nf + 0.29)' nrd='0.29 / W' nrs='0.29 / W'
+ sa=0 sb=0 sd=0 mult=1 m=1
XM38 net23 Vbn net22 GND sky130_fd_pr__nfet_01v8 L=0.5 W=6 nf=1 ad='int((nf+1)/2) * W/nf * 0.29' as='int((nf+2)/2) * W/nf * 0.29'
+ pd='2*int((nf+1)/2) * (W/nf + 0.29)' ps='2*int((nf+2)/2) * (W/nf + 0.29)' nrd='0.29 / W' nrs='0.29 / W'
+ sa=0 sb=0 sd=0 mult=1 m=1
XM39 net24 Vbn net23 GND sky130_fd_pr__nfet_01v8 L=0.5 W=6 nf=1 ad='int((nf+1)/2) * W/nf * 0.29' as='int((nf+2)/2) * W/nf * 0.29'
+ pd='2*int((nf+1)/2) * (W/nf + 0.29)' ps='2*int((nf+2)/2) * (W/nf + 0.29)' nrd='0.29 / W' nrs='0.29 / W'
+ sa=0 sb=0 sd=0 mult=1 m=1
XM40 net11 Vbn net24 GND sky130_fd_pr__nfet_01v8 L=0.5 W=6 nf=1 ad='int((nf+1)/2) * W/nf * 0.29' as='int((nf+2)/2) * W/nf * 0.29'
+ pd='2*int((nf+1)/2) * (W/nf + 0.29)' ps='2*int((nf+2)/2) * (W/nf + 0.29)' nrd='0.29 / W' nrs='0.29 / W'
+ sa=0 sb=0 sd=0 mult=1 m=1
XM41 net11 net11 net25 VDD sky130_fd_pr__pfet_01v8 L=0.5 W=6 nf=1 ad='int((nf+1)/2) * W/nf * 0.29' as='int((nf+2)/2) * W/nf * 0.29'
+ pd='2*int((nf+1)/2) * (W/nf + 0.29)' ps='2*int((nf+2)/2) * (W/nf + 0.29)' nrd='0.29 / W' nrs='0.29 / W'
+ sa=0 sb=0 sd=0 mult=1 m=1
XM42 net25 net11 net11 VDD sky130_fd_pr__pfet_01v8 L=0.5 W=6 nf=1 ad='int((nf+1)/2) * W/nf * 0.29' as='int((nf+2)/2) * W/nf * 0.29'
+ pd='2*int((nf+1)/2) * (W/nf + 0.29)' ps='2*int((nf+2)/2) * (W/nf + 0.29)' nrd='0.29 / W' nrs='0.29 / W'
+ sa=0 sb=0 sd=0 mult=1 m=1
XM43 net11 net11 net25 VDD sky130_fd_pr__pfet_01v8 L=0.5 W=6 nf=1 ad='int((nf+1)/2) * W/nf * 0.29' as='int((nf+2)/2) * W/nf * 0.29'
+ pd='2*int((nf+1)/2) * (W/nf + 0.29)' ps='2*int((nf+2)/2) * (W/nf + 0.29)' nrd='0.29 / W' nrs='0.29 / W'
+ sa=0 sb=0 sd=0 mult=1 m=1
XM44 net25 net11 net11 VDD sky130_fd_pr__pfet_01v8 L=0.5 W=6 nf=1 ad='int((nf+1)/2) * W/nf * 0.29' as='int((nf+2)/2) * W/nf * 0.29'
+ pd='2*int((nf+1)/2) * (W/nf + 0.29)' ps='2*int((nf+2)/2) * (W/nf + 0.29)' nrd='0.29 / W' nrs='0.29 / W'
+ sa=0 sb=0 sd=0 mult=1 m=1
XM45 net13 net13 net26 GND sky130_fd_pr__nfet_01v8 L=0.5 W=6 nf=1 ad='int((nf+1)/2) * W/nf * 0.29' as='int((nf+2)/2) * W/nf * 0.29'
+ pd='2*int((nf+1)/2) * (W/nf + 0.29)' ps='2*int((nf+2)/2) * (W/nf + 0.29)' nrd='0.29 / W' nrs='0.29 / W'
+ sa=0 sb=0 sd=0 mult=1 m=1
XM46 net26 net13 net13 GND sky130_fd_pr__nfet_01v8 L=0.5 W=6 nf=1 ad='int((nf+1)/2) * W/nf * 0.29' as='int((nf+2)/2) * W/nf * 0.29'
+ pd='2*int((nf+1)/2) * (W/nf + 0.29)' ps='2*int((nf+2)/2) * (W/nf + 0.29)' nrd='0.29 / W' nrs='0.29 / W'
+ sa=0 sb=0 sd=0 mult=1 m=1
XM47 net13 net13 net26 GND sky130_fd_pr__nfet_01v8 L=0.5 W=6 nf=1 ad='int((nf+1)/2) * W/nf * 0.29' as='int((nf+2)/2) * W/nf * 0.29'
+ pd='2*int((nf+1)/2) * (W/nf + 0.29)' ps='2*int((nf+2)/2) * (W/nf + 0.29)' nrd='0.29 / W' nrs='0.29 / W'
+ sa=0 sb=0 sd=0 mult=1 m=1
XM48 net26 net13 net13 GND sky130_fd_pr__nfet_01v8 L=0.5 W=6 nf=1 ad='int((nf+1)/2) * W/nf * 0.29' as='int((nf+2)/2) * W/nf * 0.29'
+ pd='2*int((nf+1)/2) * (W/nf + 0.29)' ps='2*int((nf+2)/2) * (W/nf + 0.29)' nrd='0.29 / W' nrs='0.29 / W'
+ sa=0 sb=0 sd=0 mult=1 m=1
XM49 Vcn Vbp VP VDD sky130_fd_pr__pfet_01v8 L=0.5 W=6 nf=1 ad='int((nf+1)/2) * W/nf * 0.29' as='int((nf+2)/2) * W/nf * 0.29'
+ pd='2*int((nf+1)/2) * (W/nf + 0.29)' ps='2*int((nf+2)/2) * (W/nf + 0.29)' nrd='0.29 / W' nrs='0.29 / W'
+ sa=0 sb=0 sd=0 mult=1 m=1
XM50 Vcn Vcn net26 GND sky130_fd_pr__nfet_01v8 L=0.5 W=6 nf=1 ad='int((nf+1)/2) * W/nf * 0.29' as='int((nf+2)/2) * W/nf * 0.29'
+ pd='2*int((nf+1)/2) * (W/nf + 0.29)' ps='2*int((nf+2)/2) * (W/nf + 0.29)' nrd='0.29 / W' nrs='0.29 / W'
+ sa=0 sb=0 sd=0 mult=1 m=1
XM51 VN net13 net26 GND sky130_fd_pr__nfet_01v8 L=0.5 W=6 nf=1 ad='int((nf+1)/2) * W/nf * 0.29' as='int((nf+2)/2) * W/nf * 0.29'
+ pd='2*int((nf+1)/2) * (W/nf + 0.29)' ps='2*int((nf+2)/2) * (W/nf + 0.29)' nrd='0.29 / W' nrs='0.29 / W'
+ sa=0 sb=0 sd=0 mult=1 m=1
XM52 VN Vbn Vcp GND sky130_fd_pr__nfet_01v8 L=0.5 W=6 nf=1 ad='int((nf+1)/2) * W/nf * 0.29' as='int((nf+2)/2) * W/nf * 0.29'
+ pd='2*int((nf+1)/2) * (W/nf + 0.29)' ps='2*int((nf+2)/2) * (W/nf + 0.29)' nrd='0.29 / W' nrs='0.29 / W'
+ sa=0 sb=0 sd=0 mult=1 m=1
XM53 net25 Vcp Vcp VDD sky130_fd_pr__pfet_01v8 L=0.5 W=6 nf=1 ad='int((nf+1)/2) * W/nf * 0.29' as='int((nf+2)/2) * W/nf * 0.29'
+ pd='2*int((nf+1)/2) * (W/nf + 0.29)' ps='2*int((nf+2)/2) * (W/nf + 0.29)' nrd='0.29 / W' nrs='0.29 / W'
+ sa=0 sb=0 sd=0 mult=1 m=1
XM54 net25 net11 VP VDD sky130_fd_pr__pfet_01v8 L=0.5 W=6 nf=1 ad='int((nf+1)/2) * W/nf * 0.29' as='int((nf+2)/2) * W/nf * 0.29'
+ pd='2*int((nf+1)/2) * (W/nf + 0.29)' ps='2*int((nf+2)/2) * (W/nf + 0.29)' nrd='0.29 / W' nrs='0.29 / W'
+ sa=0 sb=0 sd=0 mult=1 m=1
XM55 Vbp Vbp VP VDD sky130_fd_pr__pfet_01v8 L=0.5 W=6 nf=1 ad='int((nf+1)/2) * W/nf * 0.29' as='int((nf+2)/2) * W/nf * 0.29'
+ pd='2*int((nf+1)/2) * (W/nf + 0.29)' ps='2*int((nf+2)/2) * (W/nf + 0.29)' nrd='0.29 / W' nrs='0.29 / W'
+ sa=0 sb=0 sd=0 mult=1 m=1
XM56 VN Vbn Vbp GND sky130_fd_pr__nfet_01v8 L=0.5 W=6 nf=1 ad='int((nf+1)/2) * W/nf * 0.29' as='int((nf+2)/2) * W/nf * 0.29'
+ pd='2*int((nf+1)/2) * (W/nf + 0.29)' ps='2*int((nf+2)/2) * (W/nf + 0.29)' nrd='0.29 / W' nrs='0.29 / W'
+ sa=0 sb=0 sd=0 mult=1 m=1
XM57 Vcn VP VP VDD sky130_fd_pr__pfet_01v8 L=0.5 W=6 nf=1 ad='int((nf+1)/2) * W/nf * 0.29' as='int((nf+2)/2) * W/nf * 0.29'
+ pd='2*int((nf+1)/2) * (W/nf + 0.29)' ps='2*int((nf+2)/2) * (W/nf + 0.29)' nrd='0.29 / W' nrs='0.29 / W'
+ sa=0 sb=0 sd=0 mult=1 m=1
XM58 Vcp VP VP VDD sky130_fd_pr__pfet_01v8 L=0.5 W=6 nf=1 ad='int((nf+1)/2) * W/nf * 0.29' as='int((nf+2)/2) * W/nf * 0.29'
+ pd='2*int((nf+1)/2) * (W/nf + 0.29)' ps='2*int((nf+2)/2) * (W/nf + 0.29)' nrd='0.29 / W' nrs='0.29 / W'
+ sa=0 sb=0 sd=0 mult=1 m=1
XM59 VN VN Vcn GND sky130_fd_pr__nfet_01v8 L=0.5 W=6 nf=1 ad='int((nf+1)/2) * W/nf * 0.29' as='int((nf+2)/2) * W/nf * 0.29'
+ pd='2*int((nf+1)/2) * (W/nf + 0.29)' ps='2*int((nf+2)/2) * (W/nf + 0.29)' nrd='0.29 / W' nrs='0.29 / W'
+ sa=0 sb=0 sd=0 mult=1 m=1
XM60 VN VN Vcp GND sky130_fd_pr__nfet_01v8 L=0.5 W=6 nf=1 ad='int((nf+1)/2) * W/nf * 0.29' as='int((nf+2)/2) * W/nf * 0.29'
+ pd='2*int((nf+1)/2) * (W/nf + 0.29)' ps='2*int((nf+2)/2) * (W/nf + 0.29)' nrd='0.29 / W' nrs='0.29 / W'
+ sa=0 sb=0 sd=0 mult=1 m=1
XM61 VN VN Vcp GND sky130_fd_pr__nfet_01v8 L=0.5 W=6 nf=1 ad='int((nf+1)/2) * W/nf * 0.29' as='int((nf+2)/2) * W/nf * 0.29'
+ pd='2*int((nf+1)/2) * (W/nf + 0.29)' ps='2*int((nf+2)/2) * (W/nf + 0.29)' nrd='0.29 / W' nrs='0.29 / W'
+ sa=0 sb=0 sd=0 mult=1 m=1
XM62 VN VN Vcn GND sky130_fd_pr__nfet_01v8 L=0.5 W=6 nf=1 ad='int((nf+1)/2) * W/nf * 0.29' as='int((nf+2)/2) * W/nf * 0.29'
+ pd='2*int((nf+1)/2) * (W/nf + 0.29)' ps='2*int((nf+2)/2) * (W/nf + 0.29)' nrd='0.29 / W' nrs='0.29 / W'
+ sa=0 sb=0 sd=0 mult=1 m=1
XM63 VP VP Vcp VDD sky130_fd_pr__pfet_01v8 L=0.5 W=6 nf=1 ad='int((nf+1)/2) * W/nf * 0.29' as='int((nf+2)/2) * W/nf * 0.29'
+ pd='2*int((nf+1)/2) * (W/nf + 0.29)' ps='2*int((nf+2)/2) * (W/nf + 0.29)' nrd='0.29 / W' nrs='0.29 / W'
+ sa=0 sb=0 sd=0 mult=1 m=1
XM64 VP VP Vcn VDD sky130_fd_pr__pfet_01v8 L=0.5 W=6 nf=1 ad='int((nf+1)/2) * W/nf * 0.29' as='int((nf+2)/2) * W/nf * 0.29'
+ pd='2*int((nf+1)/2) * (W/nf + 0.29)' ps='2*int((nf+2)/2) * (W/nf + 0.29)' nrd='0.29 / W' nrs='0.29 / W'
+ sa=0 sb=0 sd=0 mult=1 m=1
.ends

.GLOBAL GND
.GLOBAL VDD
.end
